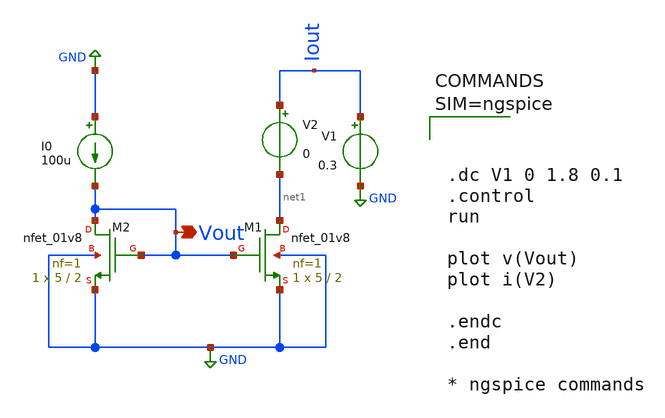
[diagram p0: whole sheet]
** sch_path: spice/cmnmos.sch
**.subckt cmnmos Vout
*.opin Vout
XM2 Vout Vout GND GND sky130_fd_pr__nfet_01v8 L=2 W=5 nf=1 ad='int((1 + 1)/2) * 5 / 1 * 0.29' as='int((1 + 2)/2) * 5 / 1 * 0.29'
+ pd='2*int((1 + 1)/2) * (5 / 1 + 0.29)' ps='2*int((1 + 2)/2) * (5 / 1 + 0.29)' nrd='0.29 / 5 ' nrs='0.29 / 5 '
+ sa=0 sb=0 sd=0 mult=1 m=1
I0 GND Vout 100u
XM1 net1 Vout GND GND sky130_fd_pr__nfet_01v8 L=2 W=5 nf=1 ad='int((1 + 1)/2) * 5 / 1 * 0.29' as='int((1 + 2)/2) * 5 / 1 * 0.29'
+ pd='2*int((1 + 1)/2) * (5 / 1 + 0.29)' ps='2*int((1 + 2)/2) * (5 / 1 + 0.29)' nrd='0.29 / 5 ' nrs='0.29 / 5 '
+ sa=0 sb=0 sd=0 mult=1 m=1
V1 Iout GND 0.3
V2 Iout net1 0
**** begin user architecture code

** opencircuitdesign pdks install
.lib $::SKYWATER_MODELS/sky130.lib.spice tt





.dc V1 0 1.8 0.1
.control
run

plot v(Vout)
plot i(V2)

.endc
.end

* ngspice commands



**** end user architecture code
**.ends
.GLOBAL GND
.end
